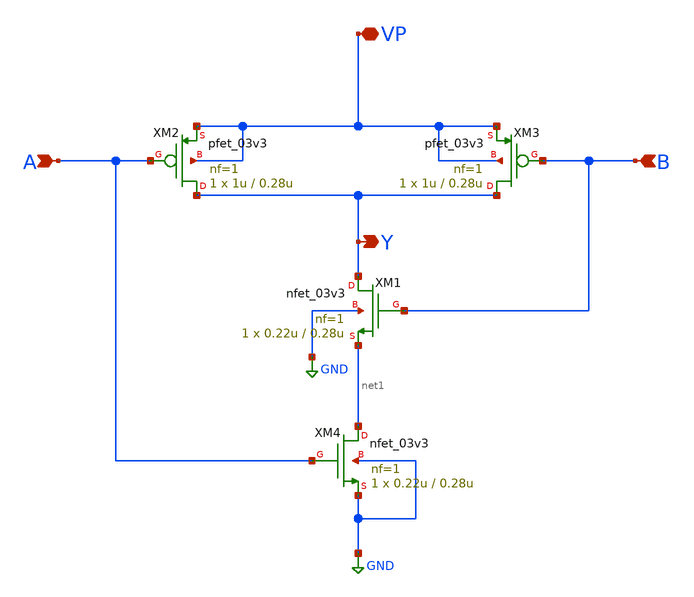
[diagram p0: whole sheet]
** sch_path: nand_gate.sch
**.subckt nand_gate A B Y VP
*.ipin A
*.ipin B
*.opin Y
*.iopin VP
XM1 Y B net1 GND nfet_03v3 L=0.28u W=0.22u nf=1 ad='int((nf+1)/2) * W/nf * 0.18u' as='int((nf+2)/2) * W/nf * 0.18u'
+ pd='2*int((nf+1)/2) * (W/nf + 0.18u)' ps='2*int((nf+2)/2) * (W/nf + 0.18u)' nrd='0.18u / W' nrs='0.18u / W'
+ sa=0 sb=0 sd=0 m=1
XM2 Y A VP VP pfet_03v3 L=0.28u W=1u nf=1 ad='int((nf+1)/2) * W/nf * 0.18u' as='int((nf+2)/2) * W/nf * 0.18u'
+ pd='2*int((nf+1)/2) * (W/nf + 0.18u)' ps='2*int((nf+2)/2) * (W/nf + 0.18u)' nrd='0.18u / W' nrs='0.18u / W'
+ sa=0 sb=0 sd=0 m=1
XM4 net1 A GND GND nfet_03v3 L=0.28u W=0.22u nf=1 ad='int((nf+1)/2) * W/nf * 0.18u' as='int((nf+2)/2) * W/nf * 0.18u'
+ pd='2*int((nf+1)/2) * (W/nf + 0.18u)' ps='2*int((nf+2)/2) * (W/nf + 0.18u)' nrd='0.18u / W' nrs='0.18u / W'
+ sa=0 sb=0 sd=0 m=1
XM3 Y B VP VP pfet_03v3 L=0.28u W=1u nf=1 ad='int((nf+1)/2) * W/nf * 0.18u' as='int((nf+2)/2) * W/nf * 0.18u'
+ pd='2*int((nf+1)/2) * (W/nf + 0.18u)' ps='2*int((nf+2)/2) * (W/nf + 0.18u)' nrd='0.18u / W' nrs='0.18u / W'
+ sa=0 sb=0 sd=0 m=1
**.ends
.GLOBAL GND
.end
